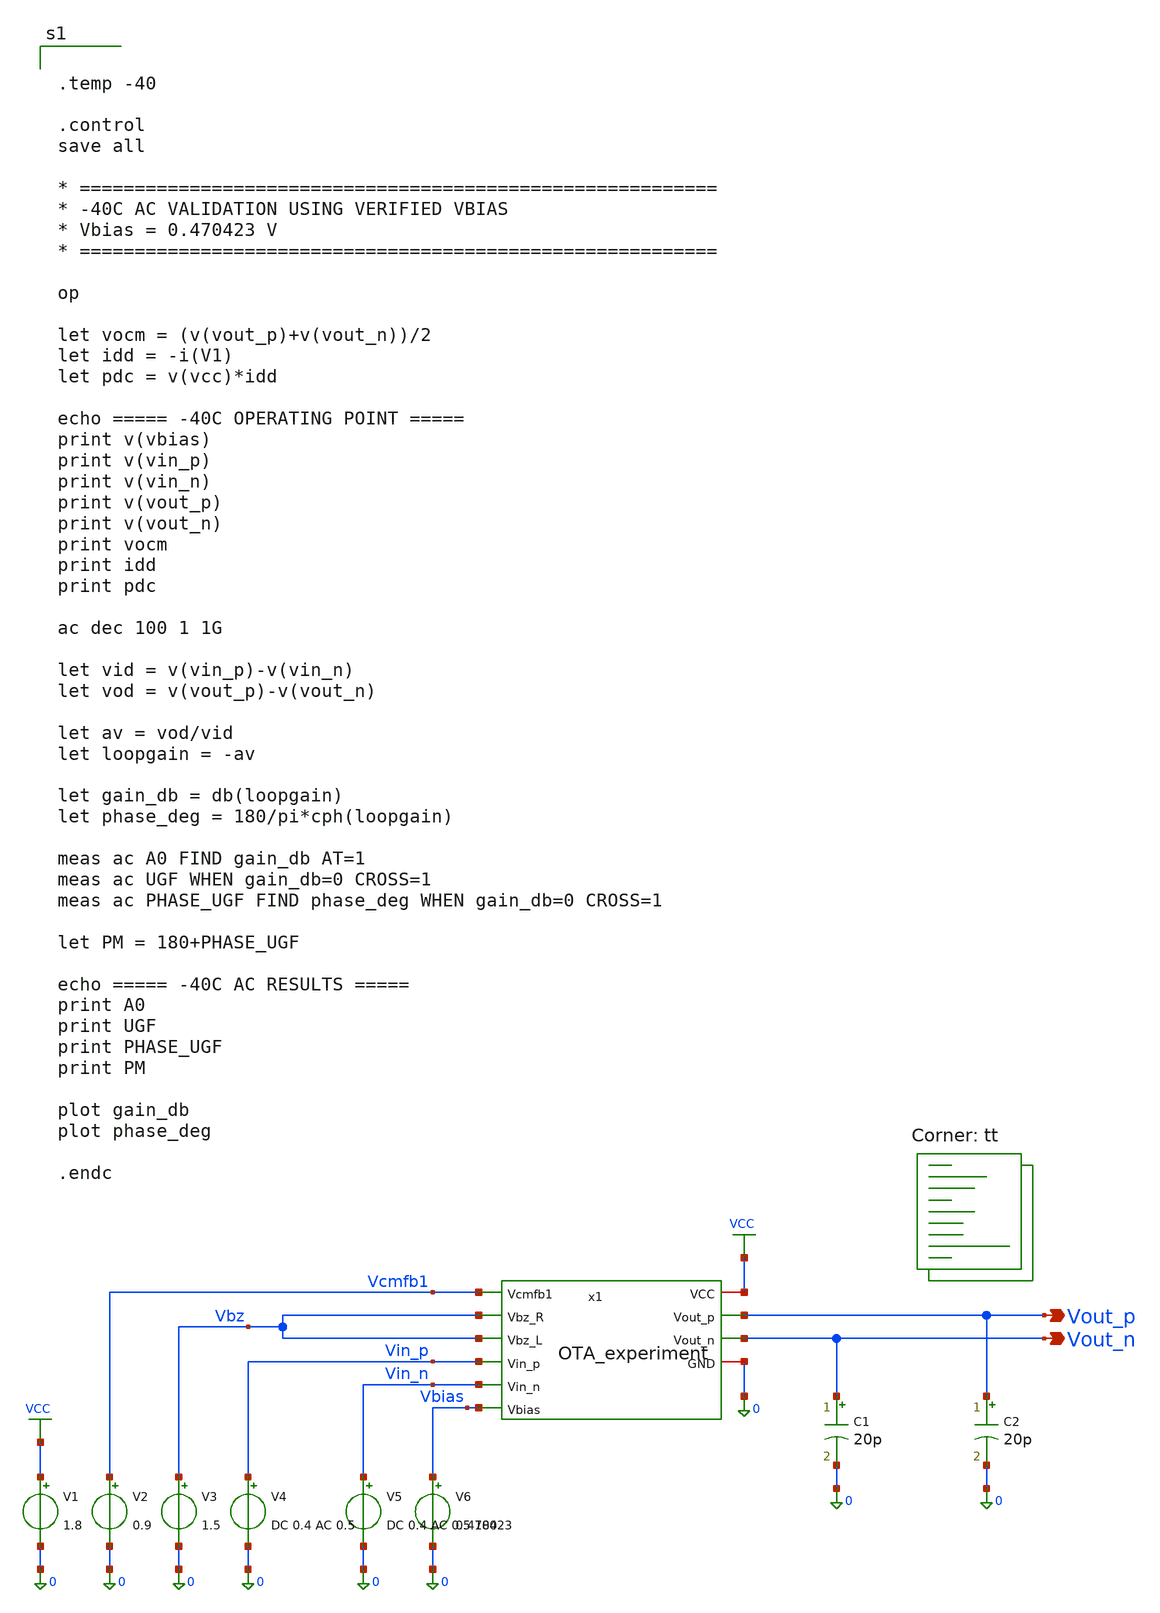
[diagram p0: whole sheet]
** sch_path: blocks/01_OTA/sim/tb_OTA_TEMP_AC_verify.sch
**.subckt tb_OTA_TEMP_AC_verify Vout_p Vout_n
*.opin Vout_p
*.opin Vout_n
V1 VCC 0 1.8
V2 Vcmfb1 0 0.9
V3 Vbz 0 1.5
V4 Vin_p 0 DC 0.4 AC 0.5
V5 Vin_n 0 DC 0.4 AC 0.5 180
V6 Vbias 0 0.470423
C1 Vout_n 0 20p m=1
C2 Vout_p 0 20p m=1
x1 VCC Vcmfb1 Vbz Vbz Vin_p Vin_n Vout_p Vout_n Vbias 0 OTA_experiment
**** begin user architecture code


.temp -40

.control
save all

* ==========================================================
* -40C AC VALIDATION USING VERIFIED VBIAS
* Vbias = 0.470423 V
* ==========================================================

op

let vocm = (v(vout_p)+v(vout_n))/2
let idd = -i(V1)
let pdc = v(vcc)*idd

echo ===== -40C OPERATING POINT =====
print v(vbias)
print v(vin_p)
print v(vin_n)
print v(vout_p)
print v(vout_n)
print vocm
print idd
print pdc

ac dec 100 1 1G

let vid = v(vin_p)-v(vin_n)
let vod = v(vout_p)-v(vout_n)

let av = vod/vid
let loopgain = -av

let gain_db = db(loopgain)
let phase_deg = 180/pi*cph(loopgain)

meas ac A0 FIND gain_db AT=1
meas ac UGF WHEN gain_db=0 CROSS=1
meas ac PHASE_UGF FIND phase_deg WHEN gain_db=0 CROSS=1

let PM = 180+PHASE_UGF

echo ===== -40C AC RESULTS =====
print A0
print UGF
print PHASE_UGF
print PM

plot gain_db
plot phase_deg

.endc


.lib $::SKYWATER_MODELS/sky130.lib.spice tt
**** end user architecture code
**.ends

* expanding   symbol:  blocks/01_OTA/xschem/OTA_experiment.sym # of pins=10
** sym_path: blocks/01_OTA/xschem/OTA_experiment.sym
** sch_path: blocks/01_OTA/xschem/OTA_experiment.sch
.subckt OTA_experiment VCC Vcmfb1 Vbz_R Vbz_L Vin_p Vin_n Vout_p Vout_n Vbias GND
*.ipin Vin_p
*.ipin Vin_n
*.ipin Vbias
*.ipin Vbz_R
*.ipin Vbz_L
*.ipin Vcmfb1
*.opin Vout_p
*.opin Vout_n
*.iopin VCC
*.iopin GND
XM1 net5 Vin_p net3 net5 sky130_fd_pr__pfet_01v8 L=1.2 W=120 nf=1 ad='int((1 + 1)/2) * 120 / 1 * 0.29'
+ as='int((1 + 2)/2) * 120 / 1 * 0.29' pd='2*int((1 + 1)/2) * (120 / 1 + 0.29)' ps='2*int((1 + 2)/2) * (120 / 1 + 0.29)'
+ nrd='0.29 / 120 ' nrs='0.29 / 120 ' sa=0 sb=0 sd=0 mult=1 m=1
XM2 net5 Vin_n net4 net5 sky130_fd_pr__pfet_01v8 L=1.2 W=120 nf=1 ad='int((1 + 1)/2) * 120 / 1 * 0.29'
+ as='int((1 + 2)/2) * 120 / 1 * 0.29' pd='2*int((1 + 1)/2) * (120 / 1 + 0.29)' ps='2*int((1 + 2)/2) * (120 / 1 + 0.29)'
+ nrd='0.29 / 120 ' nrs='0.29 / 120 ' sa=0 sb=0 sd=0 mult=1 m=1
XM3 net3 Vbias GND GND sky130_fd_pr__nfet_01v8 L=2 W=8 nf=1 ad='int((1 + 1)/2) * 8 / 1 * 0.29' as='int((1 + 2)/2) * 8 / 1 * 0.29'
+ pd='2*int((1 + 1)/2) * (8 / 1 + 0.29)' ps='2*int((1 + 2)/2) * (8 / 1 + 0.29)' nrd='0.29 / 8 ' nrs='0.29 / 8 '
+ sa=0 sb=0 sd=0 mult=1 m=1
XM4 net4 Vbias GND GND sky130_fd_pr__nfet_01v8 L=2 W=8 nf=1 ad='int((1 + 1)/2) * 8 / 1 * 0.29' as='int((1 + 2)/2) * 8 / 1 * 0.29'
+ pd='2*int((1 + 1)/2) * (8 / 1 + 0.29)' ps='2*int((1 + 2)/2) * (8 / 1 + 0.29)' nrd='0.29 / 8 ' nrs='0.29 / 8 '
+ sa=0 sb=0 sd=0 mult=1 m=1
XM5 net1 net4 GND GND sky130_fd_pr__nfet_01v8 L=2 W=20 nf=1 ad='int((1 + 1)/2) * 20 / 1 * 0.29' as='int((1 + 2)/2) * 20 / 1 * 0.29'
+ pd='2*int((1 + 1)/2) * (20 / 1 + 0.29)' ps='2*int((1 + 2)/2) * (20 / 1 + 0.29)' nrd='0.29 / 20 ' nrs='0.29 / 20 '
+ sa=0 sb=0 sd=0 mult=1 m=1
XM6 net2 net3 GND GND sky130_fd_pr__nfet_01v8 L=2 W=20 nf=1 ad='int((1 + 1)/2) * 20 / 1 * 0.29' as='int((1 + 2)/2) * 20 / 1 * 0.29'
+ pd='2*int((1 + 1)/2) * (20 / 1 + 0.29)' ps='2*int((1 + 2)/2) * (20 / 1 + 0.29)' nrd='0.29 / 20 ' nrs='0.29 / 20 '
+ sa=0 sb=0 sd=0 mult=1 m=1
XM7 VCC net1 net1 VCC sky130_fd_pr__pfet_01v8 L=2 W=30 nf=1 ad='int((1 + 1)/2) * 30 / 1 * 0.29' as='int((1 + 2)/2) * 30 / 1 * 0.29'
+ pd='2*int((1 + 1)/2) * (30 / 1 + 0.29)' ps='2*int((1 + 2)/2) * (30 / 1 + 0.29)' nrd='0.29 / 30 ' nrs='0.29 / 30 '
+ sa=0 sb=0 sd=0 mult=1 m=1
XM8 VCC net2 net2 VCC sky130_fd_pr__pfet_01v8 L=2 W=30 nf=1 ad='int((1 + 1)/2) * 30 / 1 * 0.29' as='int((1 + 2)/2) * 30 / 1 * 0.29'
+ pd='2*int((1 + 1)/2) * (30 / 1 + 0.29)' ps='2*int((1 + 2)/2) * (30 / 1 + 0.29)' nrd='0.29 / 30 ' nrs='0.29 / 30 '
+ sa=0 sb=0 sd=0 mult=1 m=1
XM9 VCC net1 Vout_p VCC sky130_fd_pr__pfet_01v8 L=1 W=300 nf=1 ad='int((1 + 1)/2) * 300 / 1 * 0.29' as='int((1 + 2)/2) * 300 / 1 * 0.29'
+ pd='2*int((1 + 1)/2) * (300 / 1 + 0.29)' ps='2*int((1 + 2)/2) * (300 / 1 + 0.29)' nrd='0.29 / 300 ' nrs='0.29 / 300 '
+ sa=0 sb=0 sd=0 mult=1 m=1
XM10 VCC net2 Vout_n VCC sky130_fd_pr__pfet_01v8 L=1 W=300 nf=1 ad='int((1 + 1)/2) * 300 / 1 * 0.29'
+ as='int((1 + 2)/2) * 300 / 1 * 0.29' pd='2*int((1 + 1)/2) * (300 / 1 + 0.29)' ps='2*int((1 + 2)/2) * (300 / 1 + 0.29)'
+ nrd='0.29 / 300 ' nrs='0.29 / 300 ' sa=0 sb=0 sd=0 mult=1 m=1
XM11 Vout_p net4 GND GND sky130_fd_pr__nfet_01v8 L=1 W=200 nf=1 ad='int((1 + 1)/2) * 200 / 1 * 0.29'
+ as='int((1 + 2)/2) * 200 / 1 * 0.29' pd='2*int((1 + 1)/2) * (200 / 1 + 0.29)' ps='2*int((1 + 2)/2) * (200 / 1 + 0.29)'
+ nrd='0.29 / 200 ' nrs='0.29 / 200 ' sa=0 sb=0 sd=0 mult=1 m=1
XM12 Vout_n net3 GND GND sky130_fd_pr__nfet_01v8 L=1 W=200 nf=1 ad='int((1 + 1)/2) * 200 / 1 * 0.29'
+ as='int((1 + 2)/2) * 200 / 1 * 0.29' pd='2*int((1 + 1)/2) * (200 / 1 + 0.29)' ps='2*int((1 + 2)/2) * (200 / 1 + 0.29)'
+ nrd='0.29 / 200 ' nrs='0.29 / 200 ' sa=0 sb=0 sd=0 mult=1 m=1
XM13 VCC Vcmfb1 net5 VCC sky130_fd_pr__pfet_01v8 L=1.2 W=60 nf=1 ad='int((1 + 1)/2) * 60 / 1 * 0.29'
+ as='int((1 + 2)/2) * 60 / 1 * 0.29' pd='2*int((1 + 1)/2) * (60 / 1 + 0.29)' ps='2*int((1 + 2)/2) * (60 / 1 + 0.29)'
+ nrd='0.29 / 60 ' nrs='0.29 / 60 ' sa=0 sb=0 sd=0 mult=1 m=1
XC1 Vout_p net4 sky130_fd_pr__cap_mim_m3_1 W=1 L=1 MF=80 m=80
XC2 net3 Vout_n sky130_fd_pr__cap_mim_m3_1 W=1 L=1 MF=80 m=80
.ends

.GLOBAL VCC
.end
